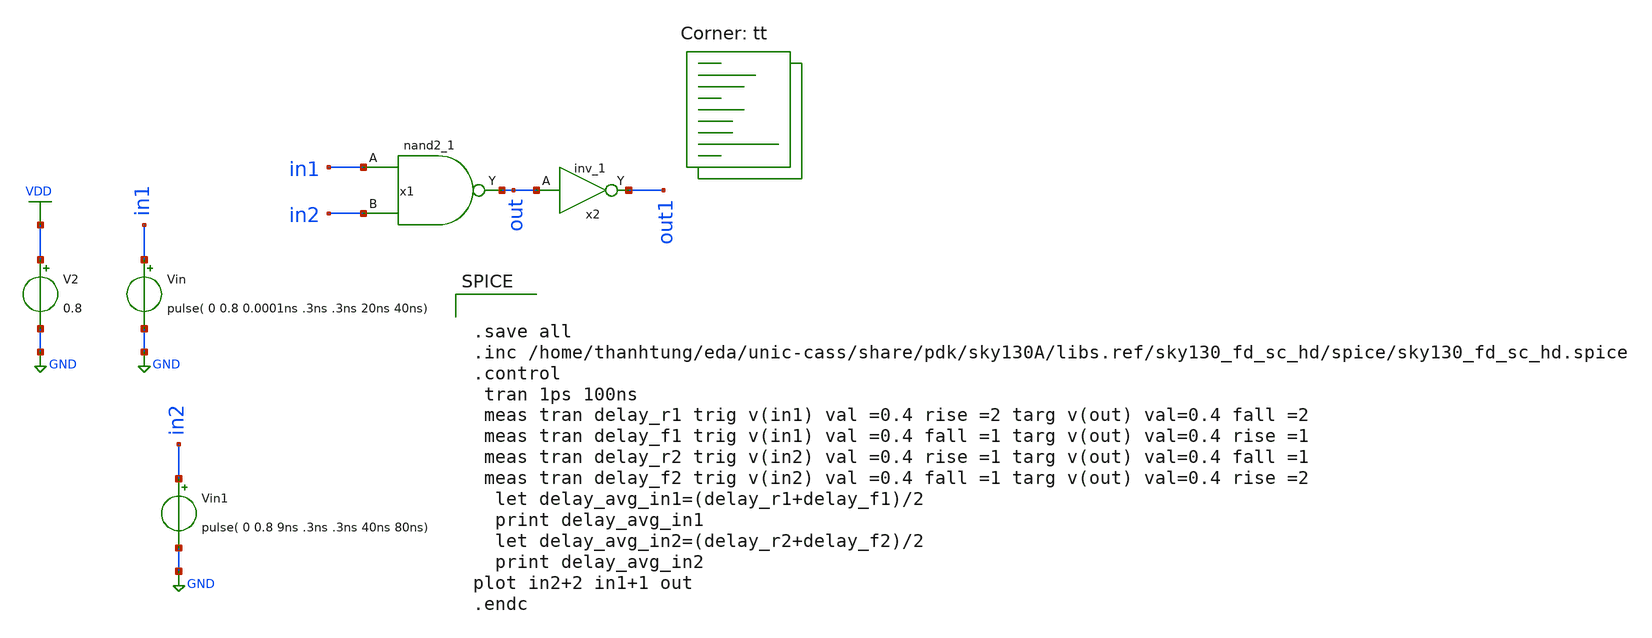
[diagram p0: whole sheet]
** sch_path: d_2nand_fan.sch
**.subckt d_2nand_fan
x1 in1 in2 GND GND VDD VDD out sky130_fd_sc_hd__nand2_1
V2 VDD GND 0.8
Vin in1 GND pulse( 0 0.8 0.0001ns .3ns .3ns 20ns 40ns)
Vin1 in2 GND pulse( 0 0.8 9ns .3ns .3ns 40ns 80ns)
x2 out GND GND VDD VDD out1 sky130_fd_sc_hd__inv_1
**** begin user architecture code


.save all
.inc /home/thanhtung/eda/unic-cass/share/pdk/sky130A/libs.ref/sky130_fd_sc_hd/spice/sky130_fd_sc_hd.spice
.control
 tran 1ps 100ns
 meas tran delay_r1 trig v(in1) val =0.4 rise =2 targ v(out) val=0.4 fall =2
 meas tran delay_f1 trig v(in1) val =0.4 fall =1 targ v(out) val=0.4 rise =1
 meas tran delay_r2 trig v(in2) val =0.4 rise =1 targ v(out) val=0.4 fall =1
 meas tran delay_f2 trig v(in2) val =0.4 fall =1 targ v(out) val=0.4 rise =2
  let delay_avg_in1=(delay_r1+delay_f1)/2
  print delay_avg_in1
  let delay_avg_in2=(delay_r2+delay_f2)/2
  print delay_avg_in2
plot in2+2 in1+1 out
.endc


.lib $::SKYWATER_MODELS/sky130.lib.spice tt
**** end user architecture code
**.ends
.GLOBAL GND
.GLOBAL VDD
.end
